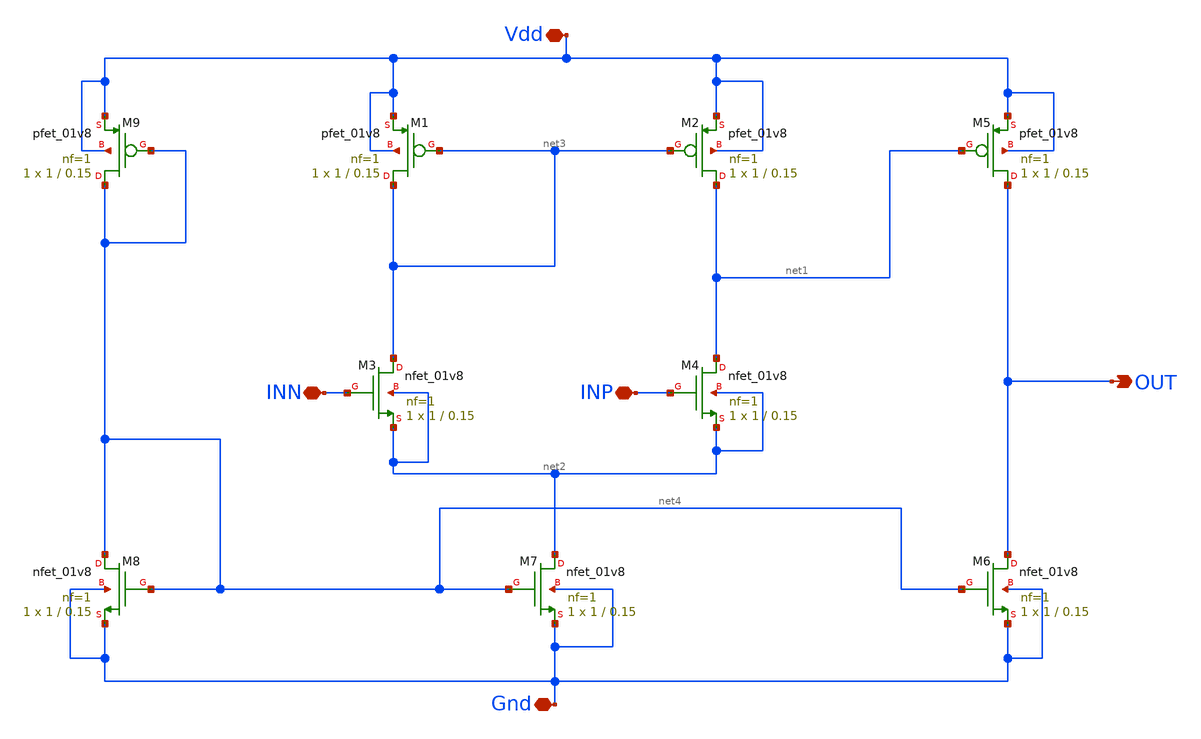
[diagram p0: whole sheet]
** sch_path: Week_4/OneBitADC_PreLayout/1_bit_ADC_sym.sch
**.subckt 1_bit_ADC_sym Vdd INN INP Gnd OUT
*.iopin Vdd
*.iopin INN
*.iopin INP
*.iopin Gnd
*.opin OUT
XM2 net1 net3 Vdd Vdd sky130_fd_pr__pfet_01v8 L=0.15 W=1 nf=1 ad='int((nf+1)/2) * W/nf * 0.29' as='int((nf+2)/2) * W/nf * 0.29'
+ pd='2*int((nf+1)/2) * (W/nf + 0.29)' ps='2*int((nf+2)/2) * (W/nf + 0.29)' nrd='0.29 / W' nrs='0.29 / W'
+ sa=0 sb=0 sd=0 mult=1 m=1
XM3 net3 INN net2 net2 sky130_fd_pr__nfet_01v8 L=0.15 W=1 nf=1 ad='int((nf+1)/2) * W/nf * 0.29' as='int((nf+2)/2) * W/nf * 0.29'
+ pd='2*int((nf+1)/2) * (W/nf + 0.29)' ps='2*int((nf+2)/2) * (W/nf + 0.29)' nrd='0.29 / W' nrs='0.29 / W'
+ sa=0 sb=0 sd=0 mult=1 m=1
XM4 net1 INP net2 net2 sky130_fd_pr__nfet_01v8 L=0.15 W=1 nf=1 ad='int((nf+1)/2) * W/nf * 0.29' as='int((nf+2)/2) * W/nf * 0.29'
+ pd='2*int((nf+1)/2) * (W/nf + 0.29)' ps='2*int((nf+2)/2) * (W/nf + 0.29)' nrd='0.29 / W' nrs='0.29 / W'
+ sa=0 sb=0 sd=0 mult=1 m=1
XM1 net3 net3 Vdd Vdd sky130_fd_pr__pfet_01v8 L=0.15 W=1 nf=1 ad='int((nf+1)/2) * W/nf * 0.29' as='int((nf+2)/2) * W/nf * 0.29'
+ pd='2*int((nf+1)/2) * (W/nf + 0.29)' ps='2*int((nf+2)/2) * (W/nf + 0.29)' nrd='0.29 / W' nrs='0.29 / W'
+ sa=0 sb=0 sd=0 mult=1 m=1
XM5 OUT net1 Vdd Vdd sky130_fd_pr__pfet_01v8 L=0.15 W=1 nf=1 ad='int((nf+1)/2) * W/nf * 0.29' as='int((nf+2)/2) * W/nf * 0.29'
+ pd='2*int((nf+1)/2) * (W/nf + 0.29)' ps='2*int((nf+2)/2) * (W/nf + 0.29)' nrd='0.29 / W' nrs='0.29 / W'
+ sa=0 sb=0 sd=0 mult=1 m=1
XM6 OUT net4 Gnd Gnd sky130_fd_pr__nfet_01v8 L=0.15 W=1 nf=1 ad='int((nf+1)/2) * W/nf * 0.29' as='int((nf+2)/2) * W/nf * 0.29'
+ pd='2*int((nf+1)/2) * (W/nf + 0.29)' ps='2*int((nf+2)/2) * (W/nf + 0.29)' nrd='0.29 / W' nrs='0.29 / W'
+ sa=0 sb=0 sd=0 mult=1 m=1
XM7 net2 net4 Gnd Gnd sky130_fd_pr__nfet_01v8 L=0.15 W=1 nf=1 ad='int((nf+1)/2) * W/nf * 0.29' as='int((nf+2)/2) * W/nf * 0.29'
+ pd='2*int((nf+1)/2) * (W/nf + 0.29)' ps='2*int((nf+2)/2) * (W/nf + 0.29)' nrd='0.29 / W' nrs='0.29 / W'
+ sa=0 sb=0 sd=0 mult=1 m=1
XM8 net4 net4 Gnd Gnd sky130_fd_pr__nfet_01v8 L=0.15 W=1 nf=1 ad='int((nf+1)/2) * W/nf * 0.29' as='int((nf+2)/2) * W/nf * 0.29'
+ pd='2*int((nf+1)/2) * (W/nf + 0.29)' ps='2*int((nf+2)/2) * (W/nf + 0.29)' nrd='0.29 / W' nrs='0.29 / W'
+ sa=0 sb=0 sd=0 mult=1 m=1
XM9 net4 net4 Vdd Vdd sky130_fd_pr__pfet_01v8 L=0.15 W=1 nf=1 ad='int((nf+1)/2) * W/nf * 0.29' as='int((nf+2)/2) * W/nf * 0.29'
+ pd='2*int((nf+1)/2) * (W/nf + 0.29)' ps='2*int((nf+2)/2) * (W/nf + 0.29)' nrd='0.29 / W' nrs='0.29 / W'
+ sa=0 sb=0 sd=0 mult=1 m=1
**.ends
.end
